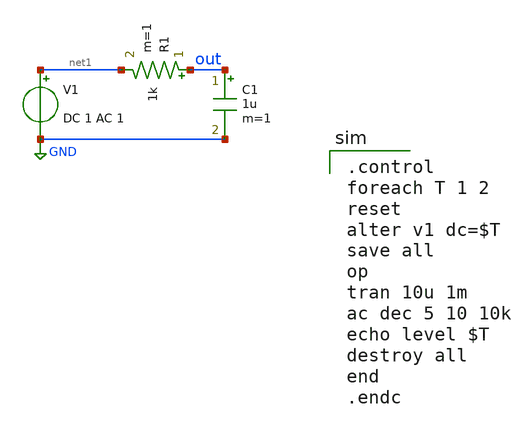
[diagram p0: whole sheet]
** sch_path: examples/xschem-analysis/rc-program.sch
**.subckt rc-program
V1 net1 GND DC 1 AC 1
R1 out net1 1k m=1
C1 out GND 1u m=1
**** begin user architecture code

.control
foreach T 1 2
reset
alter v1 dc=$T
save all
op
tran 10u 1m
ac dec 5 10 10k
echo level $T
destroy all
end
.endc

**** end user architecture code
**.ends
.GLOBAL GND
.end
